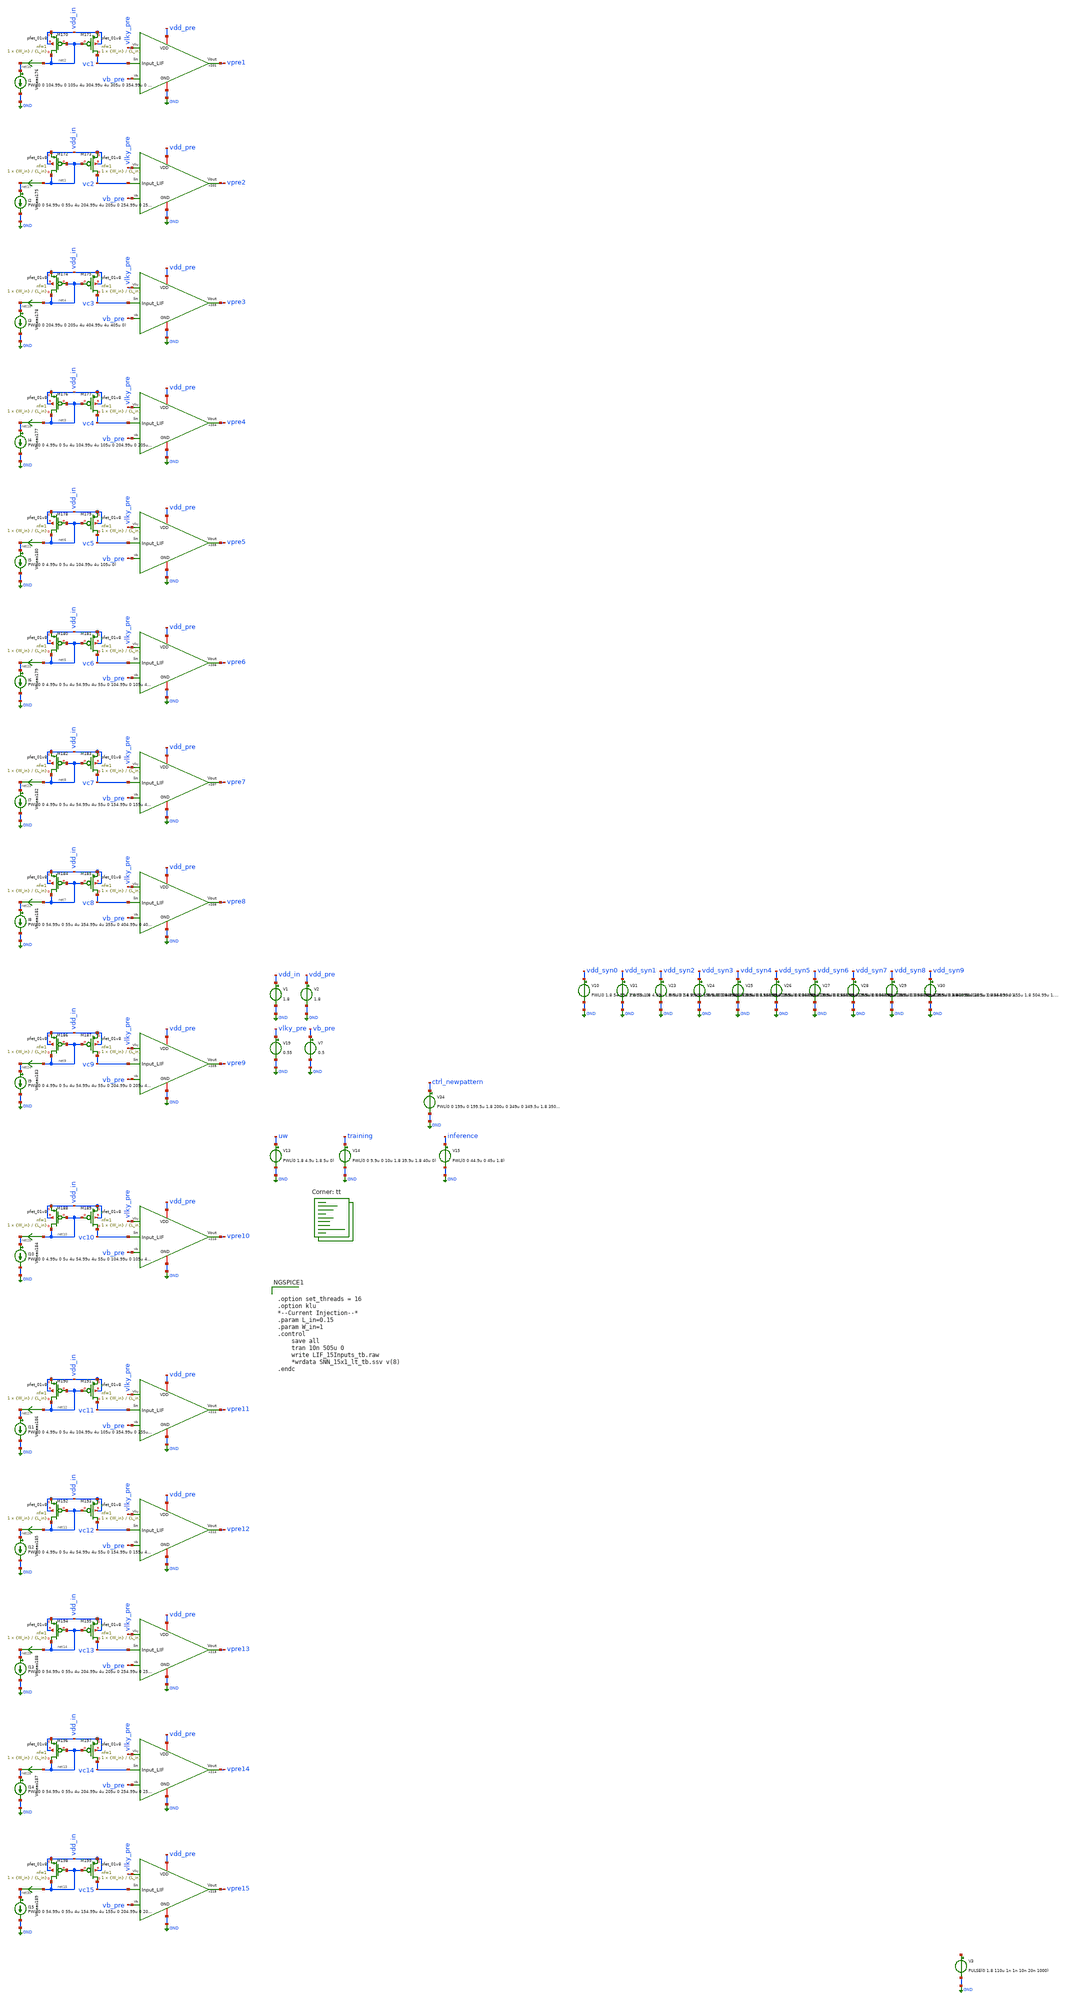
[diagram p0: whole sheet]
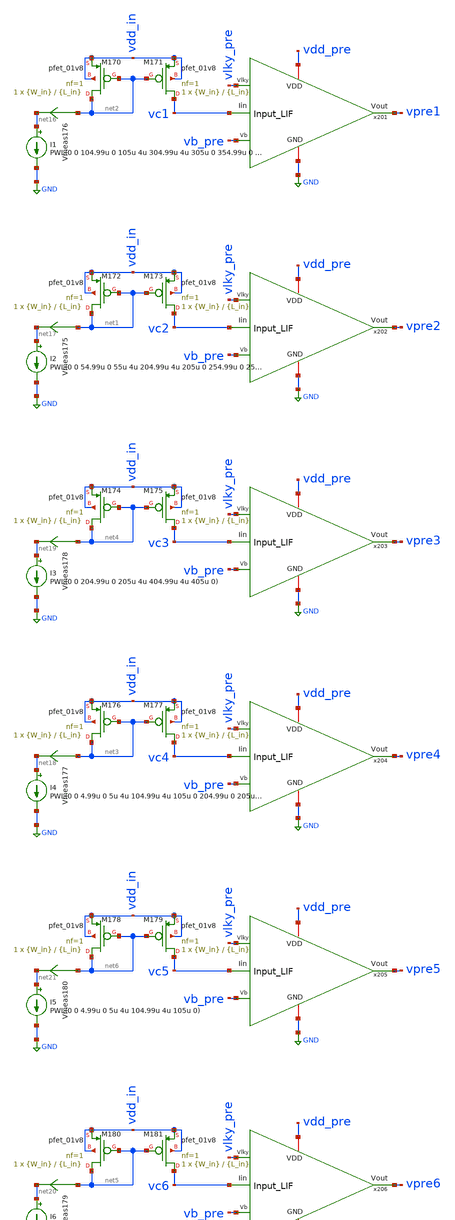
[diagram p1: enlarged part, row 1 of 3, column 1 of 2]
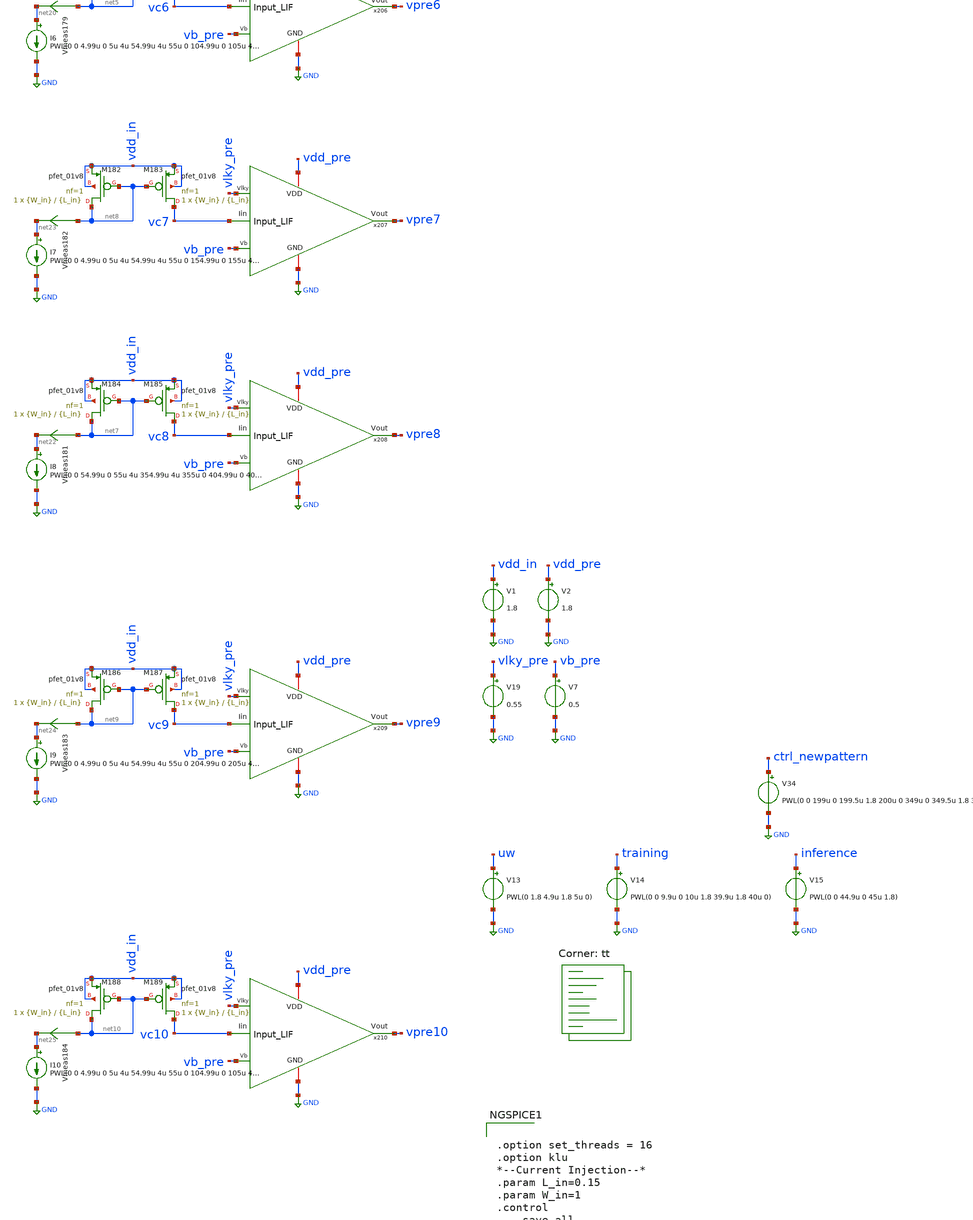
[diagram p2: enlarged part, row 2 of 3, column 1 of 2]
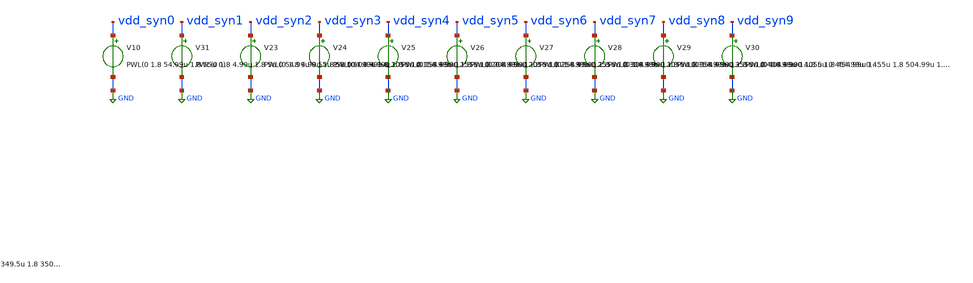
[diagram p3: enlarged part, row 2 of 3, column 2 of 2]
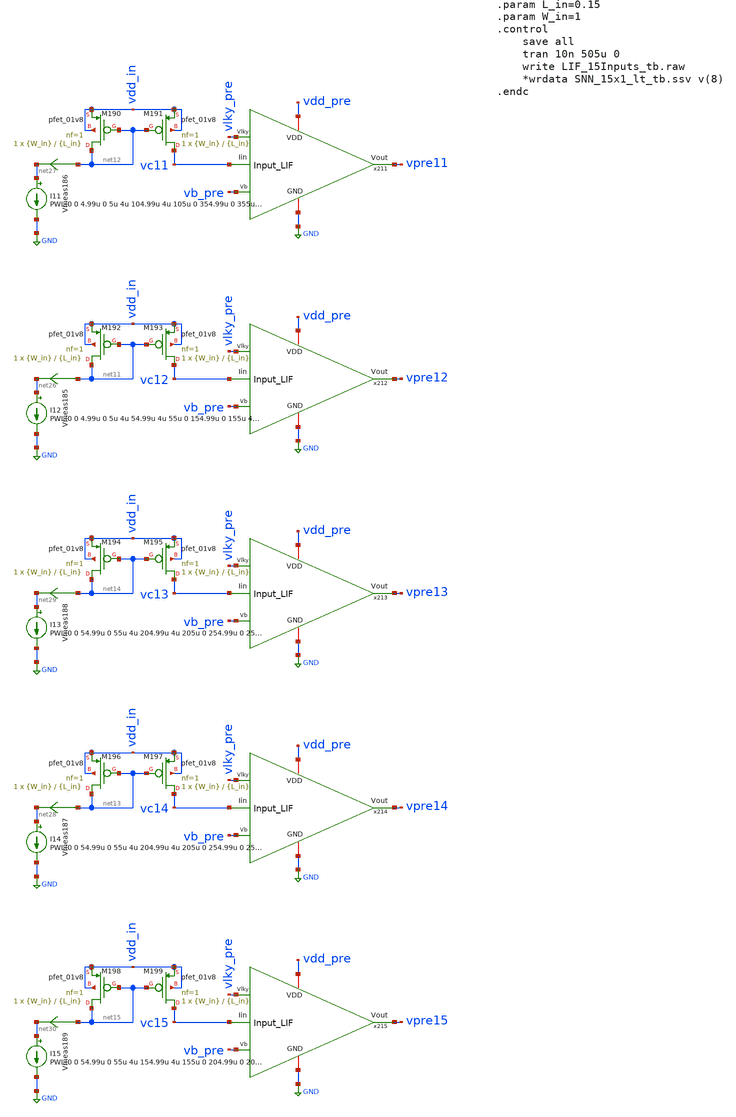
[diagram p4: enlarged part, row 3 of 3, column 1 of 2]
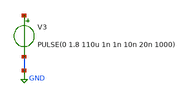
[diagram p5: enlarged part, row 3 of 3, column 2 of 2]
** sch_path: SNN/LIF_15Inputs_tb.sch
**.subckt LIF_15Inputs_tb
V1 vdd_in GND 1.8
V2 vdd_pre GND 1.8
XM173 vc2 net1 vdd_in vdd_in sky130_fd_pr__pfet_01v8 L={L_in} W={W_in} nf=1 ad='int((nf+1)/2) * W/nf * 0.29'
+ as='int((nf+2)/2) * W/nf * 0.29' pd='2*int((nf+1)/2) * (W/nf + 0.29)' ps='2*int((nf+2)/2) * (W/nf + 0.29)'
+ nrd='0.29 / W' nrs='0.29 / W' sa=0 sb=0 sd=0 mult=1 m=1
XM172 net1 net1 vdd_in vdd_in sky130_fd_pr__pfet_01v8 L={L_in} W={W_in} nf=1 ad='int((nf+1)/2) * W/nf * 0.29'
+ as='int((nf+2)/2) * W/nf * 0.29' pd='2*int((nf+1)/2) * (W/nf + 0.29)' ps='2*int((nf+2)/2) * (W/nf + 0.29)'
+ nrd='0.29 / W' nrs='0.29 / W' sa=0 sb=0 sd=0 mult=1 m=1
V13 uw GND PWL(0 1.8 4.9u 1.8 5u 0)
V14 training GND PWL(0 0 9.9u 0 10u 1.8 39.9u 1.8 40u 0)
V15 inference GND PWL(0 0 44.9u 0 45u 1.8)
V7 vb_pre GND 0.5
XM171 vc1 net2 vdd_in vdd_in sky130_fd_pr__pfet_01v8 L={L_in} W={W_in} nf=1 ad='int((nf+1)/2) * W/nf * 0.29'
+ as='int((nf+2)/2) * W/nf * 0.29' pd='2*int((nf+1)/2) * (W/nf + 0.29)' ps='2*int((nf+2)/2) * (W/nf + 0.29)'
+ nrd='0.29 / W' nrs='0.29 / W' sa=0 sb=0 sd=0 mult=1 m=1
XM170 net2 net2 vdd_in vdd_in sky130_fd_pr__pfet_01v8 L={L_in} W={W_in} nf=1 ad='int((nf+1)/2) * W/nf * 0.29'
+ as='int((nf+2)/2) * W/nf * 0.29' pd='2*int((nf+1)/2) * (W/nf + 0.29)' ps='2*int((nf+2)/2) * (W/nf + 0.29)'
+ nrd='0.29 / W' nrs='0.29 / W' sa=0 sb=0 sd=0 mult=1 m=1
V19 vlky_pre GND 0.55
XM177 vc4 net3 vdd_in vdd_in sky130_fd_pr__pfet_01v8 L={L_in} W={W_in} nf=1 ad='int((nf+1)/2) * W/nf * 0.29'
+ as='int((nf+2)/2) * W/nf * 0.29' pd='2*int((nf+1)/2) * (W/nf + 0.29)' ps='2*int((nf+2)/2) * (W/nf + 0.29)'
+ nrd='0.29 / W' nrs='0.29 / W' sa=0 sb=0 sd=0 mult=1 m=1
XM176 net3 net3 vdd_in vdd_in sky130_fd_pr__pfet_01v8 L={L_in} W={W_in} nf=1 ad='int((nf+1)/2) * W/nf * 0.29'
+ as='int((nf+2)/2) * W/nf * 0.29' pd='2*int((nf+1)/2) * (W/nf + 0.29)' ps='2*int((nf+2)/2) * (W/nf + 0.29)'
+ nrd='0.29 / W' nrs='0.29 / W' sa=0 sb=0 sd=0 mult=1 m=1
XM175 vc3 net4 vdd_in vdd_in sky130_fd_pr__pfet_01v8 L={L_in} W={W_in} nf=1 ad='int((nf+1)/2) * W/nf * 0.29'
+ as='int((nf+2)/2) * W/nf * 0.29' pd='2*int((nf+1)/2) * (W/nf + 0.29)' ps='2*int((nf+2)/2) * (W/nf + 0.29)'
+ nrd='0.29 / W' nrs='0.29 / W' sa=0 sb=0 sd=0 mult=1 m=1
XM174 net4 net4 vdd_in vdd_in sky130_fd_pr__pfet_01v8 L={L_in} W={W_in} nf=1 ad='int((nf+1)/2) * W/nf * 0.29'
+ as='int((nf+2)/2) * W/nf * 0.29' pd='2*int((nf+1)/2) * (W/nf + 0.29)' ps='2*int((nf+2)/2) * (W/nf + 0.29)'
+ nrd='0.29 / W' nrs='0.29 / W' sa=0 sb=0 sd=0 mult=1 m=1
XM181 vc6 net5 vdd_in vdd_in sky130_fd_pr__pfet_01v8 L={L_in} W={W_in} nf=1 ad='int((nf+1)/2) * W/nf * 0.29'
+ as='int((nf+2)/2) * W/nf * 0.29' pd='2*int((nf+1)/2) * (W/nf + 0.29)' ps='2*int((nf+2)/2) * (W/nf + 0.29)'
+ nrd='0.29 / W' nrs='0.29 / W' sa=0 sb=0 sd=0 mult=1 m=1
XM180 net5 net5 vdd_in vdd_in sky130_fd_pr__pfet_01v8 L={L_in} W={W_in} nf=1 ad='int((nf+1)/2) * W/nf * 0.29'
+ as='int((nf+2)/2) * W/nf * 0.29' pd='2*int((nf+1)/2) * (W/nf + 0.29)' ps='2*int((nf+2)/2) * (W/nf + 0.29)'
+ nrd='0.29 / W' nrs='0.29 / W' sa=0 sb=0 sd=0 mult=1 m=1
XM179 vc5 net6 vdd_in vdd_in sky130_fd_pr__pfet_01v8 L={L_in} W={W_in} nf=1 ad='int((nf+1)/2) * W/nf * 0.29'
+ as='int((nf+2)/2) * W/nf * 0.29' pd='2*int((nf+1)/2) * (W/nf + 0.29)' ps='2*int((nf+2)/2) * (W/nf + 0.29)'
+ nrd='0.29 / W' nrs='0.29 / W' sa=0 sb=0 sd=0 mult=1 m=1
XM178 net6 net6 vdd_in vdd_in sky130_fd_pr__pfet_01v8 L={L_in} W={W_in} nf=1 ad='int((nf+1)/2) * W/nf * 0.29'
+ as='int((nf+2)/2) * W/nf * 0.29' pd='2*int((nf+1)/2) * (W/nf + 0.29)' ps='2*int((nf+2)/2) * (W/nf + 0.29)'
+ nrd='0.29 / W' nrs='0.29 / W' sa=0 sb=0 sd=0 mult=1 m=1
XM185 vc8 net7 vdd_in vdd_in sky130_fd_pr__pfet_01v8 L={L_in} W={W_in} nf=1 ad='int((nf+1)/2) * W/nf * 0.29'
+ as='int((nf+2)/2) * W/nf * 0.29' pd='2*int((nf+1)/2) * (W/nf + 0.29)' ps='2*int((nf+2)/2) * (W/nf + 0.29)'
+ nrd='0.29 / W' nrs='0.29 / W' sa=0 sb=0 sd=0 mult=1 m=1
XM184 net7 net7 vdd_in vdd_in sky130_fd_pr__pfet_01v8 L={L_in} W={W_in} nf=1 ad='int((nf+1)/2) * W/nf * 0.29'
+ as='int((nf+2)/2) * W/nf * 0.29' pd='2*int((nf+1)/2) * (W/nf + 0.29)' ps='2*int((nf+2)/2) * (W/nf + 0.29)'
+ nrd='0.29 / W' nrs='0.29 / W' sa=0 sb=0 sd=0 mult=1 m=1
XM183 vc7 net8 vdd_in vdd_in sky130_fd_pr__pfet_01v8 L={L_in} W={W_in} nf=1 ad='int((nf+1)/2) * W/nf * 0.29'
+ as='int((nf+2)/2) * W/nf * 0.29' pd='2*int((nf+1)/2) * (W/nf + 0.29)' ps='2*int((nf+2)/2) * (W/nf + 0.29)'
+ nrd='0.29 / W' nrs='0.29 / W' sa=0 sb=0 sd=0 mult=1 m=1
XM182 net8 net8 vdd_in vdd_in sky130_fd_pr__pfet_01v8 L={L_in} W={W_in} nf=1 ad='int((nf+1)/2) * W/nf * 0.29'
+ as='int((nf+2)/2) * W/nf * 0.29' pd='2*int((nf+1)/2) * (W/nf + 0.29)' ps='2*int((nf+2)/2) * (W/nf + 0.29)'
+ nrd='0.29 / W' nrs='0.29 / W' sa=0 sb=0 sd=0 mult=1 m=1
XM187 vc9 net9 vdd_in vdd_in sky130_fd_pr__pfet_01v8 L={L_in} W={W_in} nf=1 ad='int((nf+1)/2) * W/nf * 0.29'
+ as='int((nf+2)/2) * W/nf * 0.29' pd='2*int((nf+1)/2) * (W/nf + 0.29)' ps='2*int((nf+2)/2) * (W/nf + 0.29)'
+ nrd='0.29 / W' nrs='0.29 / W' sa=0 sb=0 sd=0 mult=1 m=1
XM186 net9 net9 vdd_in vdd_in sky130_fd_pr__pfet_01v8 L={L_in} W={W_in} nf=1 ad='int((nf+1)/2) * W/nf * 0.29'
+ as='int((nf+2)/2) * W/nf * 0.29' pd='2*int((nf+1)/2) * (W/nf + 0.29)' ps='2*int((nf+2)/2) * (W/nf + 0.29)'
+ nrd='0.29 / W' nrs='0.29 / W' sa=0 sb=0 sd=0 mult=1 m=1
XM189 vc10 net10 vdd_in vdd_in sky130_fd_pr__pfet_01v8 L={L_in} W={W_in} nf=1 ad='int((nf+1)/2) * W/nf * 0.29'
+ as='int((nf+2)/2) * W/nf * 0.29' pd='2*int((nf+1)/2) * (W/nf + 0.29)' ps='2*int((nf+2)/2) * (W/nf + 0.29)'
+ nrd='0.29 / W' nrs='0.29 / W' sa=0 sb=0 sd=0 mult=1 m=1
XM188 net10 net10 vdd_in vdd_in sky130_fd_pr__pfet_01v8 L={L_in} W={W_in} nf=1 ad='int((nf+1)/2) * W/nf * 0.29'
+ as='int((nf+2)/2) * W/nf * 0.29' pd='2*int((nf+1)/2) * (W/nf + 0.29)' ps='2*int((nf+2)/2) * (W/nf + 0.29)'
+ nrd='0.29 / W' nrs='0.29 / W' sa=0 sb=0 sd=0 mult=1 m=1
XM193 vc12 net11 vdd_in vdd_in sky130_fd_pr__pfet_01v8 L={L_in} W={W_in} nf=1 ad='int((nf+1)/2) * W/nf * 0.29'
+ as='int((nf+2)/2) * W/nf * 0.29' pd='2*int((nf+1)/2) * (W/nf + 0.29)' ps='2*int((nf+2)/2) * (W/nf + 0.29)'
+ nrd='0.29 / W' nrs='0.29 / W' sa=0 sb=0 sd=0 mult=1 m=1
XM192 net11 net11 vdd_in vdd_in sky130_fd_pr__pfet_01v8 L={L_in} W={W_in} nf=1 ad='int((nf+1)/2) * W/nf * 0.29'
+ as='int((nf+2)/2) * W/nf * 0.29' pd='2*int((nf+1)/2) * (W/nf + 0.29)' ps='2*int((nf+2)/2) * (W/nf + 0.29)'
+ nrd='0.29 / W' nrs='0.29 / W' sa=0 sb=0 sd=0 mult=1 m=1
XM191 vc11 net12 vdd_in vdd_in sky130_fd_pr__pfet_01v8 L={L_in} W={W_in} nf=1 ad='int((nf+1)/2) * W/nf * 0.29'
+ as='int((nf+2)/2) * W/nf * 0.29' pd='2*int((nf+1)/2) * (W/nf + 0.29)' ps='2*int((nf+2)/2) * (W/nf + 0.29)'
+ nrd='0.29 / W' nrs='0.29 / W' sa=0 sb=0 sd=0 mult=1 m=1
XM190 net12 net12 vdd_in vdd_in sky130_fd_pr__pfet_01v8 L={L_in} W={W_in} nf=1 ad='int((nf+1)/2) * W/nf * 0.29'
+ as='int((nf+2)/2) * W/nf * 0.29' pd='2*int((nf+1)/2) * (W/nf + 0.29)' ps='2*int((nf+2)/2) * (W/nf + 0.29)'
+ nrd='0.29 / W' nrs='0.29 / W' sa=0 sb=0 sd=0 mult=1 m=1
XM197 vc14 net13 vdd_in vdd_in sky130_fd_pr__pfet_01v8 L={L_in} W={W_in} nf=1 ad='int((nf+1)/2) * W/nf * 0.29'
+ as='int((nf+2)/2) * W/nf * 0.29' pd='2*int((nf+1)/2) * (W/nf + 0.29)' ps='2*int((nf+2)/2) * (W/nf + 0.29)'
+ nrd='0.29 / W' nrs='0.29 / W' sa=0 sb=0 sd=0 mult=1 m=1
XM196 net13 net13 vdd_in vdd_in sky130_fd_pr__pfet_01v8 L={L_in} W={W_in} nf=1 ad='int((nf+1)/2) * W/nf * 0.29'
+ as='int((nf+2)/2) * W/nf * 0.29' pd='2*int((nf+1)/2) * (W/nf + 0.29)' ps='2*int((nf+2)/2) * (W/nf + 0.29)'
+ nrd='0.29 / W' nrs='0.29 / W' sa=0 sb=0 sd=0 mult=1 m=1
XM195 vc13 net14 vdd_in vdd_in sky130_fd_pr__pfet_01v8 L={L_in} W={W_in} nf=1 ad='int((nf+1)/2) * W/nf * 0.29'
+ as='int((nf+2)/2) * W/nf * 0.29' pd='2*int((nf+1)/2) * (W/nf + 0.29)' ps='2*int((nf+2)/2) * (W/nf + 0.29)'
+ nrd='0.29 / W' nrs='0.29 / W' sa=0 sb=0 sd=0 mult=1 m=1
XM194 net14 net14 vdd_in vdd_in sky130_fd_pr__pfet_01v8 L={L_in} W={W_in} nf=1 ad='int((nf+1)/2) * W/nf * 0.29'
+ as='int((nf+2)/2) * W/nf * 0.29' pd='2*int((nf+1)/2) * (W/nf + 0.29)' ps='2*int((nf+2)/2) * (W/nf + 0.29)'
+ nrd='0.29 / W' nrs='0.29 / W' sa=0 sb=0 sd=0 mult=1 m=1
XM199 vc15 net15 vdd_in vdd_in sky130_fd_pr__pfet_01v8 L={L_in} W={W_in} nf=1 ad='int((nf+1)/2) * W/nf * 0.29'
+ as='int((nf+2)/2) * W/nf * 0.29' pd='2*int((nf+1)/2) * (W/nf + 0.29)' ps='2*int((nf+2)/2) * (W/nf + 0.29)'
+ nrd='0.29 / W' nrs='0.29 / W' sa=0 sb=0 sd=0 mult=1 m=1
XM198 net15 net15 vdd_in vdd_in sky130_fd_pr__pfet_01v8 L={L_in} W={W_in} nf=1 ad='int((nf+1)/2) * W/nf * 0.29'
+ as='int((nf+2)/2) * W/nf * 0.29' pd='2*int((nf+1)/2) * (W/nf + 0.29)' ps='2*int((nf+2)/2) * (W/nf + 0.29)'
+ nrd='0.29 / W' nrs='0.29 / W' sa=0 sb=0 sd=0 mult=1 m=1
V34 ctrl_newpattern GND PWL(0 0 199u 0 199.5u 1.8 200u 0 349u 0 349.5u 1.8 350u 0 499u 0 499.5u 1.8
+ 500u 0 649u 0 649.5u 1.8 650u 0 799u 0 799.5u 1.8 800u 0 949u 0 949.5u 1.8 950u 0 1099u 0 1099.5u 1.8
+ 1100u 0 1249u 0 1249.5u 1.8 1250u 0 1399u 0 1399.5u 1.8 1400u 0)
x201 vlky_pre vb_pre vdd_pre vpre1 GND vc1 Input_LIF
x202 vlky_pre vb_pre vdd_pre vpre2 GND vc2 Input_LIF
x203 vlky_pre vb_pre vdd_pre vpre3 GND vc3 Input_LIF
x204 vlky_pre vb_pre vdd_pre vpre4 GND vc4 Input_LIF
x205 vlky_pre vb_pre vdd_pre vpre5 GND vc5 Input_LIF
x206 vlky_pre vb_pre vdd_pre vpre6 GND vc6 Input_LIF
x207 vlky_pre vb_pre vdd_pre vpre7 GND vc7 Input_LIF
x208 vlky_pre vb_pre vdd_pre vpre8 GND vc8 Input_LIF
x209 vlky_pre vb_pre vdd_pre vpre9 GND vc9 Input_LIF
x210 vlky_pre vb_pre vdd_pre vpre10 GND vc10 Input_LIF
x211 vlky_pre vb_pre vdd_pre vpre11 GND vc11 Input_LIF
x212 vlky_pre vb_pre vdd_pre vpre12 GND vc12 Input_LIF
x213 vlky_pre vb_pre vdd_pre vpre13 GND vc13 Input_LIF
x214 vlky_pre vb_pre vdd_pre vpre14 GND vc14 Input_LIF
x215 vlky_pre vb_pre vdd_pre vpre15 GND vc15 Input_LIF
I1 net16 GND PWL(0 0 104.99u 0 105u 4u 304.99u 4u 305u 0 354.99u 0 355u 4u 404.99u 4u 405u 0)
Vmeas176 net2 net16 0
.save i(vmeas176)
I2 net17 GND PWL(0 0 54.99u 0 55u 4u 204.99u 4u 205u 0 254.99u 0 255u 4u)
Vmeas175 net1 net17 0
.save i(vmeas175)
I4 net18 GND PWL(0 0 4.99u 0 5u 4u 104.99u 4u 105u 0 204.99u 0 205u 4u 354.99u 4u 355u 0 404.99u 0
+ 405u 4u)
Vmeas177 net3 net18 0
.save i(vmeas177)
I3 net19 GND PWL(0 0 204.99u 0 205u 4u 404.99u 4u 405u 0)
Vmeas178 net4 net19 0
.save i(vmeas178)
I6 net20 GND PWL(0 0 4.99u 0 5u 4u 54.99u 4u 55u 0 104.99u 0 105u 4u 254.99u 4u 255u 0 354.99u 0
+ 355u 4u)
Vmeas179 net5 net20 0
.save i(vmeas179)
I5 net21 GND PWL(0 0 4.99u 0 5u 4u 104.99u 4u 105u 0)
Vmeas180 net6 net21 0
.save i(vmeas180)
I8 net22 GND PWL(0 0 54.99u 0 55u 4u 354.99u 4u 355u 0 404.99u 0 405u 4u)
Vmeas181 net7 net22 0
.save i(vmeas181)
I7 net23 GND PWL(0 0 4.99u 0 5u 4u 54.99u 4u 55u 0 154.99u 0 155u 4u 204.99u 4u 205u 0 304.99u 0
+ 305u 4u 354.99u 4u 355u 0)
Vmeas182 net8 net23 0
.save i(vmeas182)
I9 net24 GND PWL(0 0 4.99u 0 5u 4u 54.99u 4u 55u 0 204.99u 0 205u 4u 254.99u 4u 255u 0 354.99u 0
+ 355u 4u 404.99u 4u 405u 0 454.99u 0 455u 4u)
Vmeas183 net9 net24 0
.save i(vmeas183)
I10 net25 GND PWL(0 0 4.99u 0 5u 4u 54.99u 4u 55u 0 104.99u 0 105u 4u 154.99u 4u 155u 0 304.99u 0
+ 305u 4u 354.99u 4u 355u 0 404.99u 0 405u 4u 454.99u 4u 455u 0)
Vmeas184 net10 net25 0
.save i(vmeas184)
I12 net26 GND PWL(0 0 4.99u 0 5u 4u 54.99u 4u 55u 0 154.99u 0 155u 4u 354.99u 4u 355u 0 404.99u 0
+ 405u 4u)
Vmeas185 net11 net26 0
.save i(vmeas185)
I11 net27 GND PWL(0 0 4.99u 0 5u 4u 104.99u 4u 105u 0 354.99u 0 355u 4u 404.99u 4u 405u 0)
Vmeas186 net12 net27 0
.save i(vmeas186)
I14 net28 GND PWL(0 0 54.99u 0 55u 4u 204.99u 4u 205u 0 254.99u 0 255u 4u 354.99u 4u 355u 0 404.99u
+ 0 405u 4u 454.99u 4u 455u 0)
Vmeas187 net13 net28 0
.save i(vmeas187)
I13 net29 GND PWL(0 0 54.99u 0 55u 4u 204.99u 4u 205u 0 254.99u 0 255u 4u 304.99u 4u 305u 0 354.99u
+ 0 355u 4u 404.99u 4u 405u 0)
Vmeas188 net14 net29 0
.save i(vmeas188)
I15 net30 GND PWL(0 0 54.99u 0 55u 4u 154.99u 4u 155u 0 204.99u 0 205u 4u 254.99u 4u 255u 0 454.99u
+ 0 455u 4u)
Vmeas189 net15 net30 0
.save i(vmeas189)
V10 vdd_syn0 GND PWL(0 1.8 54.99u 1.8 55u 0)
V23 vdd_syn2 GND PWL(0 1.8 4.99u 1.8 5u 0 104.99u 0 105u 1.8 154.99u 1.8 155u 0)
V24 vdd_syn3 GND PWL(0 1.8 4.99u 1.8 5u 0 154.99u 0 155u 1.8 204.99u 1.8 205u 0)
V25 vdd_syn4 GND PWL(0 1.8 4.99u 1.8 5u 0 204.99u 0 205u 1.8 254.99u 1.8 255u 0)
V26 vdd_syn5 GND PWL(0 1.8 4.99u 1.8 5u 0 254.99u 0 255u 1.8 304.99u 1.8 305u 0)
V27 vdd_syn6 GND PWL(0 1.8 4.99u 1.8 5u 0 304.99u 0 305u 1.8 354.99u 1.8 355u 0)
V28 vdd_syn7 GND PWL(0 1.8 4.99u 1.8 5u 0 354.99u 0 355u 1.8 404.99u 1.8 405u 0)
V29 vdd_syn8 GND PWL(0 1.8 4.99u 1.8 5u 0 404.99u 0 405u 1.8 454.99u 1.8 455u 0)
V30 vdd_syn9 GND PWL(0 1.8 4.99u 1.8 5u 0 454.99u 0 455u 1.8 504.99u 1.8 505u 0)
V31 vdd_syn1 GND PWL(0 1.8 4.99u 1.8 5u 0 54.99u 0 55u 1.8 104.99u 1.8 105u 0)
V3 net31 GND PULSE(0 1.8 110u 1n 1n 10n 20n 1000)
**** begin user architecture code
.lib $::SKYWATER_MODELS/sky130.lib.spice tt

** opencircuitdesign pdks install
.inc $::SKYWATER_MODELS/rram_v0.spice



.option set_threads = 16
.option klu
*--Current Injection--*
.param L_in=0.15
.param W_in=1
.control
	save all
	tran 10n 505u 0
	write LIF_15Inputs_tb.raw
	*wrdata SNN_15x1_lt_tb.ssv v(8)
.endc


**** end user architecture code
**.ends

* expanding   symbol:  /home/ricardo/RATT_repos/Proyectos_xschem/SNN/Input_LIF.sym # of pins=6
** sym_path: Final_Design/Input_LIF.sym
** sch_path: Final_Design/Input_LIF.sch
.subckt Input_LIF Vlky Vb VDD Vout GND Iin
*.iopin GND
*.ipin Vb
*.iopin VDD
*.opin Vout
*.ipin Iin
*.ipin Vlky
XM5 net3 Vb GND GND sky130_fd_pr__nfet_01v8 L=0.15 W=5 nf=1 ad='int((nf+1)/2) * W/nf * 0.29' as='int((nf+2)/2) * W/nf * 0.29'
+ pd='2*int((nf+1)/2) * (W/nf + 0.29)' ps='2*int((nf+2)/2) * (W/nf + 0.29)' nrd='0.29 / W' nrs='0.29 / W'
+ sa=0 sb=0 sd=0 mult=1 m=1
XM4 net1 net2 net3 GND sky130_fd_pr__nfet_01v8 L=0.15 W=1.5 nf=1 ad='int((nf+1)/2) * W/nf * 0.29' as='int((nf+2)/2) * W/nf * 0.29'
+ pd='2*int((nf+1)/2) * (W/nf + 0.29)' ps='2*int((nf+2)/2) * (W/nf + 0.29)' nrd='0.29 / W' nrs='0.29 / W'
+ sa=0 sb=0 sd=0 mult=1 m=1
XM3 net1 net2 VDD VDD sky130_fd_pr__pfet_01v8 L=20 W=1 nf=1 ad='int((nf+1)/2) * W/nf * 0.29' as='int((nf+2)/2) * W/nf * 0.29'
+ pd='2*int((nf+1)/2) * (W/nf + 0.29)' ps='2*int((nf+2)/2) * (W/nf + 0.29)' nrd='0.29 / W' nrs='0.29 / W'
+ sa=0 sb=0 sd=0 mult=1 m=1
XC2 net1 GND sky130_fd_pr__cap_mim_m3_1 W=10 L=5 MF=1 m=1
XM2 Iin net1 GND GND sky130_fd_pr__nfet_01v8 L=20 W=1 nf=1 ad='int((nf+1)/2) * W/nf * 0.29' as='int((nf+2)/2) * W/nf * 0.29'
+ pd='2*int((nf+1)/2) * (W/nf + 0.29)' ps='2*int((nf+2)/2) * (W/nf + 0.29)' nrd='0.29 / W' nrs='0.29 / W'
+ sa=0 sb=0 sd=0 mult=1 m=1
XC1 Iin GND sky130_fd_pr__cap_mim_m3_1 W=20 L=20 MF=1 m=1
XM10 net4 Vout GND GND sky130_fd_pr__nfet_01v8 L=0.15 W=1.5 nf=1 ad='int((nf+1)/2) * W/nf * 0.29' as='int((nf+2)/2) * W/nf * 0.29'
+ pd='2*int((nf+1)/2) * (W/nf + 0.29)' ps='2*int((nf+2)/2) * (W/nf + 0.29)' nrd='0.29 / W' nrs='0.29 / W'
+ sa=0 sb=0 sd=0 mult=1 m=1
XM7 net2 Iin net4 GND sky130_fd_pr__nfet_01v8 L=0.15 W=1.5 nf=1 ad='int((nf+1)/2) * W/nf * 0.29' as='int((nf+2)/2) * W/nf * 0.29'
+ pd='2*int((nf+1)/2) * (W/nf + 0.29)' ps='2*int((nf+2)/2) * (W/nf + 0.29)' nrd='0.29 / W' nrs='0.29 / W'
+ sa=0 sb=0 sd=0 mult=1 m=1
XM6 net2 Iin VDD VDD sky130_fd_pr__pfet_01v8 L=0.15 W=1.5 nf=1 ad='int((nf+1)/2) * W/nf * 0.29' as='int((nf+2)/2) * W/nf * 0.29'
+ pd='2*int((nf+1)/2) * (W/nf + 0.29)' ps='2*int((nf+2)/2) * (W/nf + 0.29)' nrd='0.29 / W' nrs='0.29 / W'
+ sa=0 sb=0 sd=0 mult=1 m=1
XM9 Vout net2 net4 GND sky130_fd_pr__nfet_01v8 L=0.15 W=1.5 nf=1 ad='int((nf+1)/2) * W/nf * 0.29' as='int((nf+2)/2) * W/nf * 0.29'
+ pd='2*int((nf+1)/2) * (W/nf + 0.29)' ps='2*int((nf+2)/2) * (W/nf + 0.29)' nrd='0.29 / W' nrs='0.29 / W'
+ sa=0 sb=0 sd=0 mult=1 m=1
XM8 Vout net2 VDD VDD sky130_fd_pr__pfet_01v8 L=0.15 W=5 nf=1 ad='int((nf+1)/2) * W/nf * 0.29' as='int((nf+2)/2) * W/nf * 0.29'
+ pd='2*int((nf+1)/2) * (W/nf + 0.29)' ps='2*int((nf+2)/2) * (W/nf + 0.29)' nrd='0.29 / W' nrs='0.29 / W'
+ sa=0 sb=0 sd=0 mult=1 m=1
XM1 Iin Vlky GND GND sky130_fd_pr__nfet_01v8 L=0.15 W=1.5 nf=1 ad='int((nf+1)/2) * W/nf * 0.29' as='int((nf+2)/2) * W/nf * 0.29'
+ pd='2*int((nf+1)/2) * (W/nf + 0.29)' ps='2*int((nf+2)/2) * (W/nf + 0.29)' nrd='0.29 / W' nrs='0.29 / W'
+ sa=0 sb=0 sd=0 mult=1 m=1
.ends

.GLOBAL GND
.end
